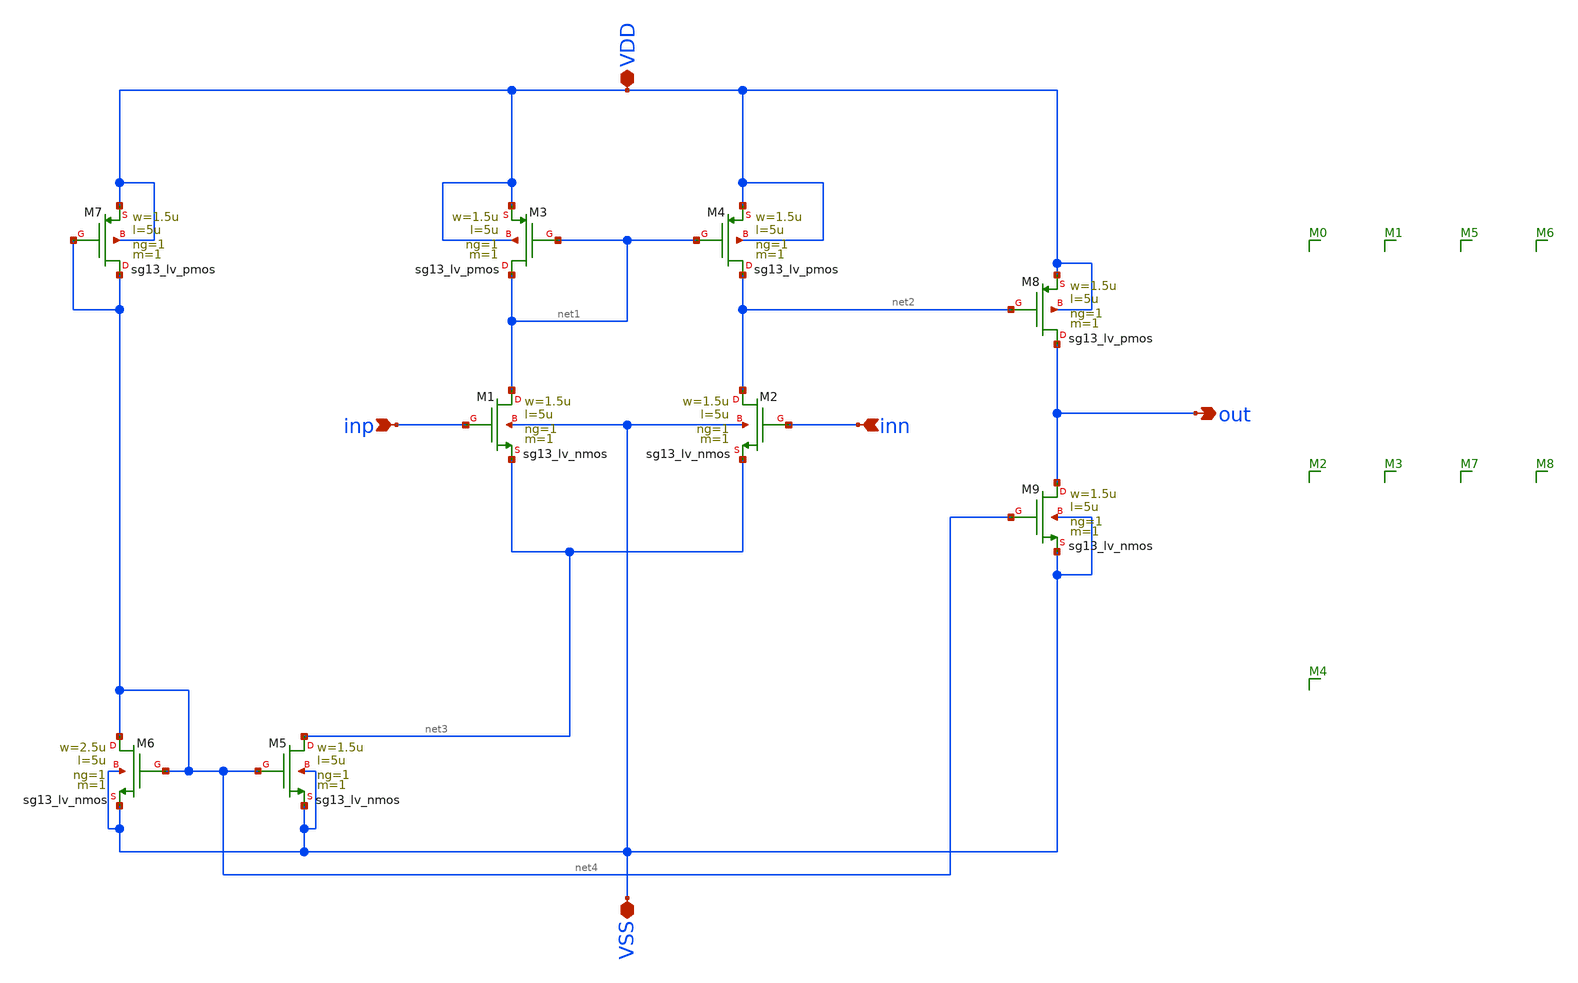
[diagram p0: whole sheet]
** sch_path: xschem/comparator.sch
**.subckt comparator inp inn VDD VSS out
*.ipin inp
*.ipin inn
*.iopin VDD
*.iopin VSS
*.opin out
XM4 net2 net1 VDD VDD sg13_lv_pmos w=1.5u l=5u ng=1 m=1 mm_ok=1
XM3 net1 net1 VDD VDD sg13_lv_pmos w=1.5u l=5u ng=1 m=1 mm_ok=1
XM1 net1 inp net3 VSS sg13_lv_nmos w=1.5u l=5u ng=1 m=1 mm_ok=1
XM2 net2 inn net3 VSS sg13_lv_nmos w=1.5u l=5u ng=1 m=1 mm_ok=1
XM7 net4 net4 VDD VDD sg13_lv_pmos w=1.5u l=5u ng=1 m=1 mm_ok=1
XM8 out net2 VDD VDD sg13_lv_pmos w=1.5u l=5u ng=1 m=1 mm_ok=1
XM6 net4 net4 VSS VSS sg13_lv_nmos w=2.5u l=5u ng=1 m=1 mm_ok=1
XM5 net3 net4 VSS VSS sg13_lv_nmos w=1.5u l=5u ng=1 m=1 mm_ok=1
XM9 out net4 VSS VSS sg13_lv_nmos w=1.5u l=5u ng=1 m=1 mm_ok=1
**.ends
.end
